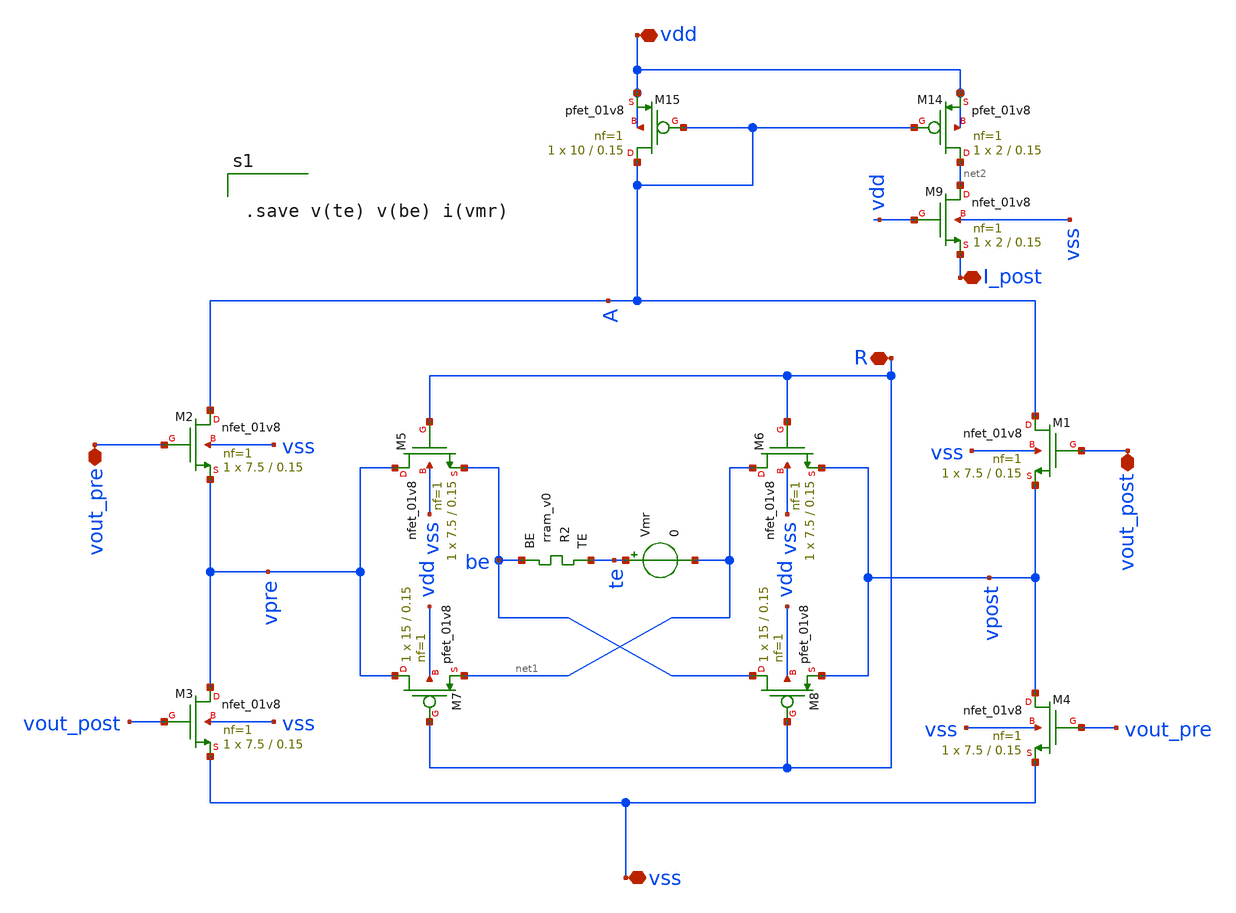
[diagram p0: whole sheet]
** sch_path: Synapse/rstdp_mirror.sch
**.subckt rstdp_mirror vdd vss R vout_post vout_pre I_post
*.iopin vdd
*.iopin vss
*.iopin R
*.iopin vout_post
*.iopin vout_pre
*.iopin I_post
XM2 A vout_pre vpre vss sky130_fd_pr__nfet_01v8 L=0.15 W=7.5 nf=1 ad='int((nf+1)/2) * W/nf * 0.29' as='int((nf+2)/2) * W/nf * 0.29'
+ pd='2*int((nf+1)/2) * (W/nf + 0.29)' ps='2*int((nf+2)/2) * (W/nf + 0.29)' nrd='0.29 / W' nrs='0.29 / W'
+ sa=0 sb=0 sd=0 mult=1 m=1
XM3 vpre vout_post vss vss sky130_fd_pr__nfet_01v8 L=0.15 W=7.5 nf=1 ad='int((nf+1)/2) * W/nf * 0.29'
+ as='int((nf+2)/2) * W/nf * 0.29' pd='2*int((nf+1)/2) * (W/nf + 0.29)' ps='2*int((nf+2)/2) * (W/nf + 0.29)'
+ nrd='0.29 / W' nrs='0.29 / W' sa=0 sb=0 sd=0 mult=1 m=1
XM1 A vout_post vpost vss sky130_fd_pr__nfet_01v8 L=0.15 W=7.5 nf=1 ad='int((nf+1)/2) * W/nf * 0.29'
+ as='int((nf+2)/2) * W/nf * 0.29' pd='2*int((nf+1)/2) * (W/nf + 0.29)' ps='2*int((nf+2)/2) * (W/nf + 0.29)'
+ nrd='0.29 / W' nrs='0.29 / W' sa=0 sb=0 sd=0 mult=1 m=1
XM4 vpost vout_pre vss vss sky130_fd_pr__nfet_01v8 L=0.15 W=7.5 nf=1 ad='int((nf+1)/2) * W/nf * 0.29'
+ as='int((nf+2)/2) * W/nf * 0.29' pd='2*int((nf+1)/2) * (W/nf + 0.29)' ps='2*int((nf+2)/2) * (W/nf + 0.29)'
+ nrd='0.29 / W' nrs='0.29 / W' sa=0 sb=0 sd=0 mult=1 m=1
XR2 te be rram_v0
XM5 vpre R be vss sky130_fd_pr__nfet_01v8 L=0.15 W=7.5 nf=1 ad='int((nf+1)/2) * W/nf * 0.29' as='int((nf+2)/2) * W/nf * 0.29'
+ pd='2*int((nf+1)/2) * (W/nf + 0.29)' ps='2*int((nf+2)/2) * (W/nf + 0.29)' nrd='0.29 / W' nrs='0.29 / W'
+ sa=0 sb=0 sd=0 mult=1 m=1
XM6 net1 R vpost vss sky130_fd_pr__nfet_01v8 L=0.15 W=7.5 nf=1 ad='int((nf+1)/2) * W/nf * 0.29' as='int((nf+2)/2) * W/nf * 0.29'
+ pd='2*int((nf+1)/2) * (W/nf + 0.29)' ps='2*int((nf+2)/2) * (W/nf + 0.29)' nrd='0.29 / W' nrs='0.29 / W'
+ sa=0 sb=0 sd=0 mult=1 m=1
XM7 vpre R net1 vdd sky130_fd_pr__pfet_01v8 L=0.15 W=15 nf=1 ad='int((nf+1)/2) * W/nf * 0.29' as='int((nf+2)/2) * W/nf * 0.29'
+ pd='2*int((nf+1)/2) * (W/nf + 0.29)' ps='2*int((nf+2)/2) * (W/nf + 0.29)' nrd='0.29 / W' nrs='0.29 / W'
+ sa=0 sb=0 sd=0 mult=1 m=1
XM8 be R vpost vdd sky130_fd_pr__pfet_01v8 L=0.15 W=15 nf=1 ad='int((nf+1)/2) * W/nf * 0.29' as='int((nf+2)/2) * W/nf * 0.29'
+ pd='2*int((nf+1)/2) * (W/nf + 0.29)' ps='2*int((nf+2)/2) * (W/nf + 0.29)' nrd='0.29 / W' nrs='0.29 / W'
+ sa=0 sb=0 sd=0 mult=1 m=1
XM14 net2 A vdd vdd sky130_fd_pr__pfet_01v8 L=0.15 W=2 nf=1 ad='int((nf+1)/2) * W/nf * 0.29' as='int((nf+2)/2) * W/nf * 0.29'
+ pd='2*int((nf+1)/2) * (W/nf + 0.29)' ps='2*int((nf+2)/2) * (W/nf + 0.29)' nrd='0.29 / W' nrs='0.29 / W'
+ sa=0 sb=0 sd=0 mult=1 m=1
XM15 A A vdd vdd sky130_fd_pr__pfet_01v8 L=0.15 W=10 nf=1 ad='int((nf+1)/2) * W/nf * 0.29' as='int((nf+2)/2) * W/nf * 0.29'
+ pd='2*int((nf+1)/2) * (W/nf + 0.29)' ps='2*int((nf+2)/2) * (W/nf + 0.29)' nrd='0.29 / W' nrs='0.29 / W'
+ sa=0 sb=0 sd=0 mult=1 m=1
Vmr te net1 0
.save i(vmr)
XM9 net2 vdd I_post vss sky130_fd_pr__nfet_01v8 L=0.15 W=2 nf=1 ad='int((nf+1)/2) * W/nf * 0.29' as='int((nf+2)/2) * W/nf * 0.29'
+ pd='2*int((nf+1)/2) * (W/nf + 0.29)' ps='2*int((nf+2)/2) * (W/nf + 0.29)' nrd='0.29 / W' nrs='0.29 / W'
+ sa=0 sb=0 sd=0 mult=1 m=1
**** begin user architecture code


.save v(te) v(be) i(vmr)


**** end user architecture code
**.ends
.end
